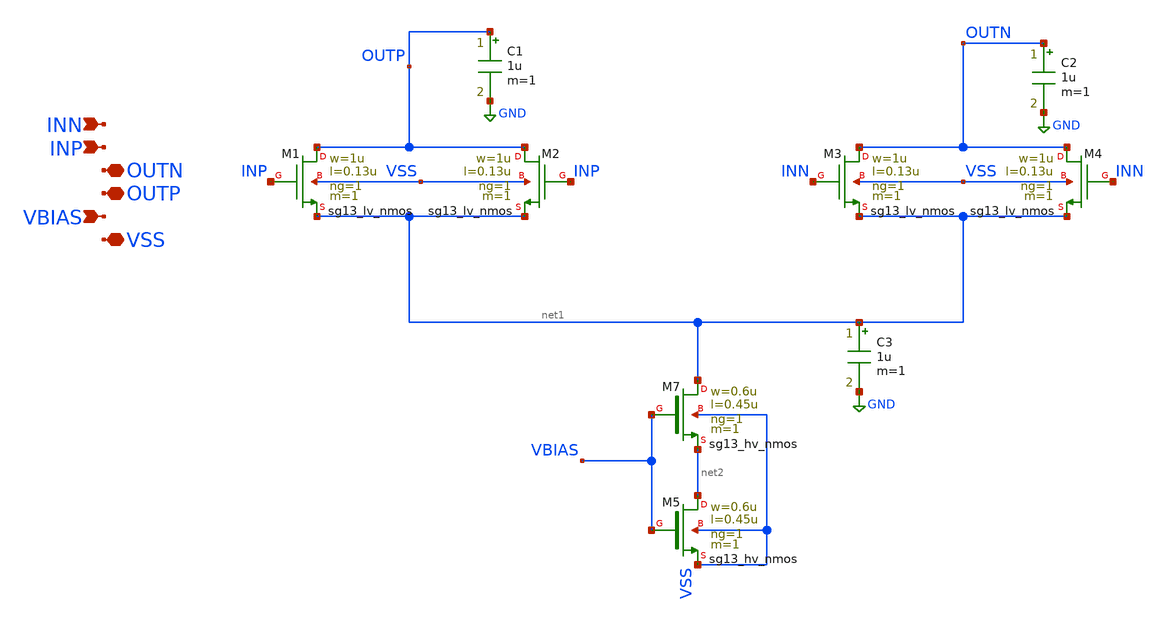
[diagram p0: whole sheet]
** sch_path: klayout/xschem/CS_Switch_2x.sch
**.subckt CS_Switch_2x VSS VBIAS OUTP OUTN INP INN
*.iopin VSS
*.ipin VBIAS
*.iopin OUTP
*.iopin OUTN
*.ipin INP
*.ipin INN
XM1 OUTP INP net1 VSS sg13_lv_nmos w=1u l=0.13u ng=1 m=1 mm_ok=1
XM2 OUTP INP net1 VSS sg13_lv_nmos w=1u l=0.13u ng=1 m=1 mm_ok=1
XM3 OUTN INN net1 VSS sg13_lv_nmos w=1u l=0.13u ng=1 m=1 mm_ok=1
XM4 OUTN INN net1 VSS sg13_lv_nmos w=1u l=0.13u ng=1 m=1 mm_ok=1
XM7 net1 VBIAS net2 VSS sg13_hv_nmos w=0.6u l=0.45u ng=1 m=1 mm_ok=1
XM5 net2 VBIAS VSS VSS sg13_hv_nmos w=0.6u l=0.45u ng=1 m=1 mm_ok=1
C1 OUTP GND 1u m=1
C2 OUTN GND 1u m=1
C3 net1 GND 1u m=1
**.ends
.GLOBAL GND
.end
